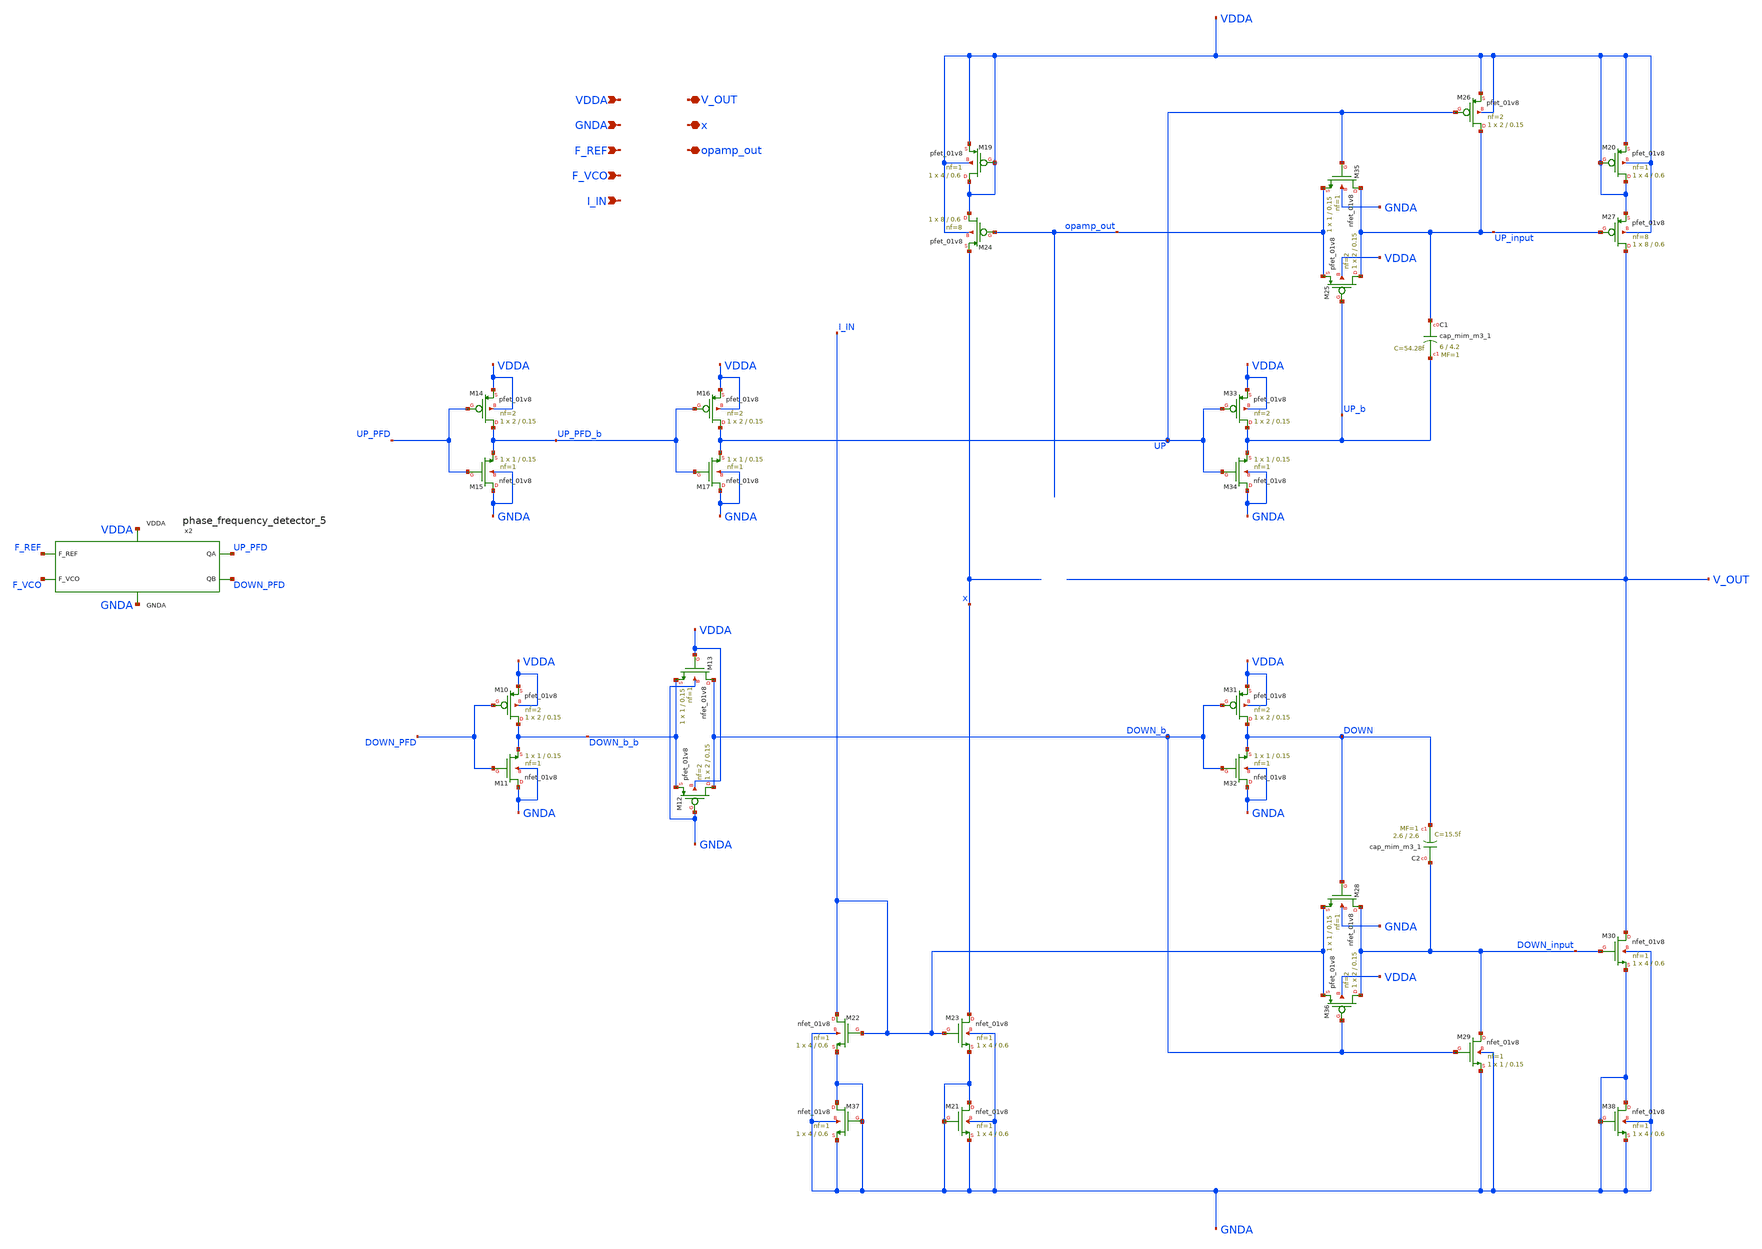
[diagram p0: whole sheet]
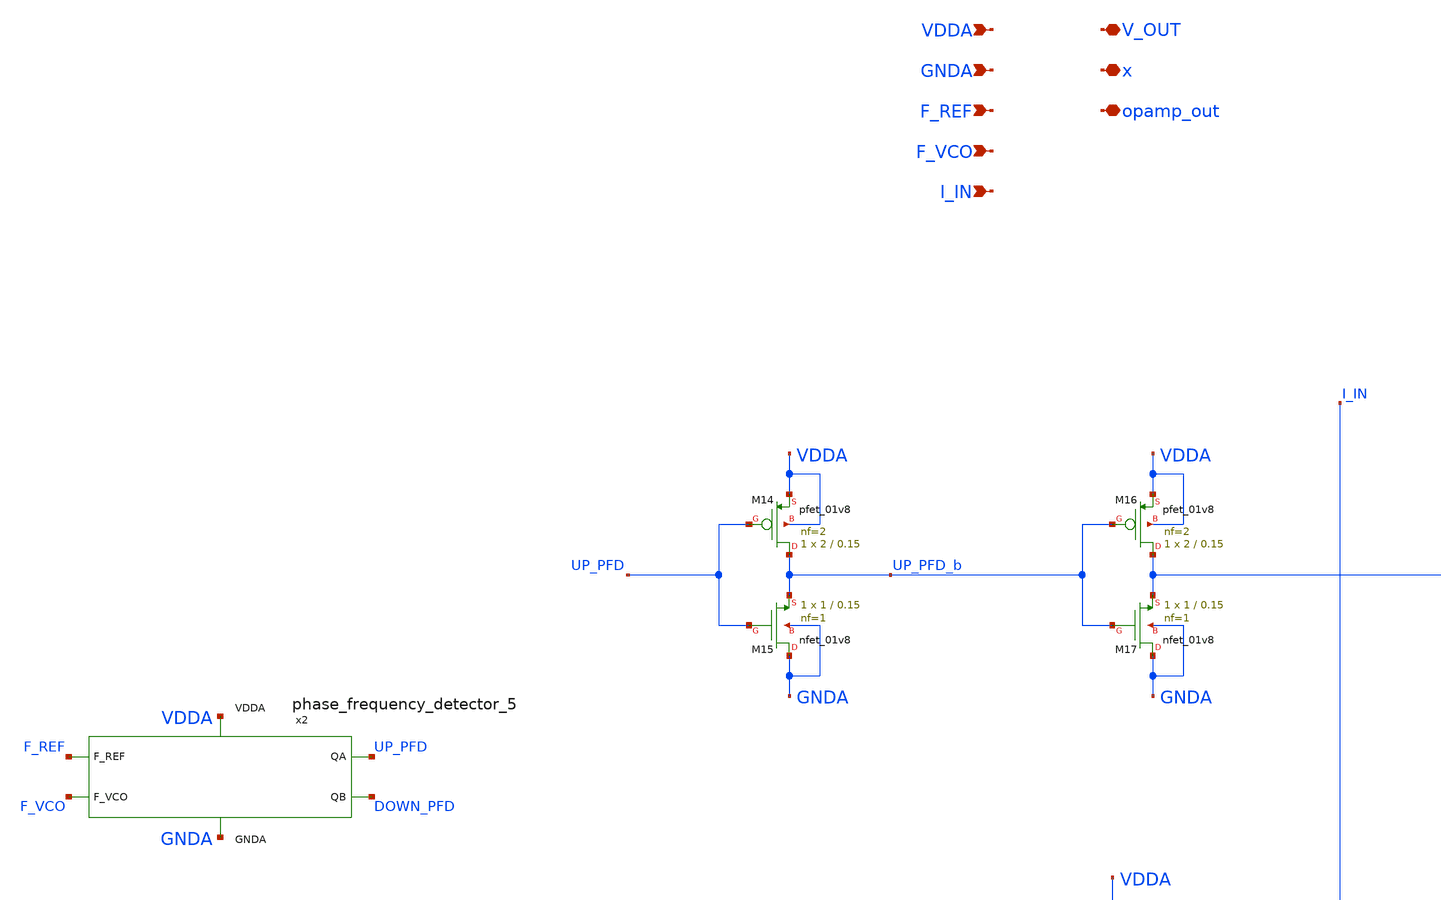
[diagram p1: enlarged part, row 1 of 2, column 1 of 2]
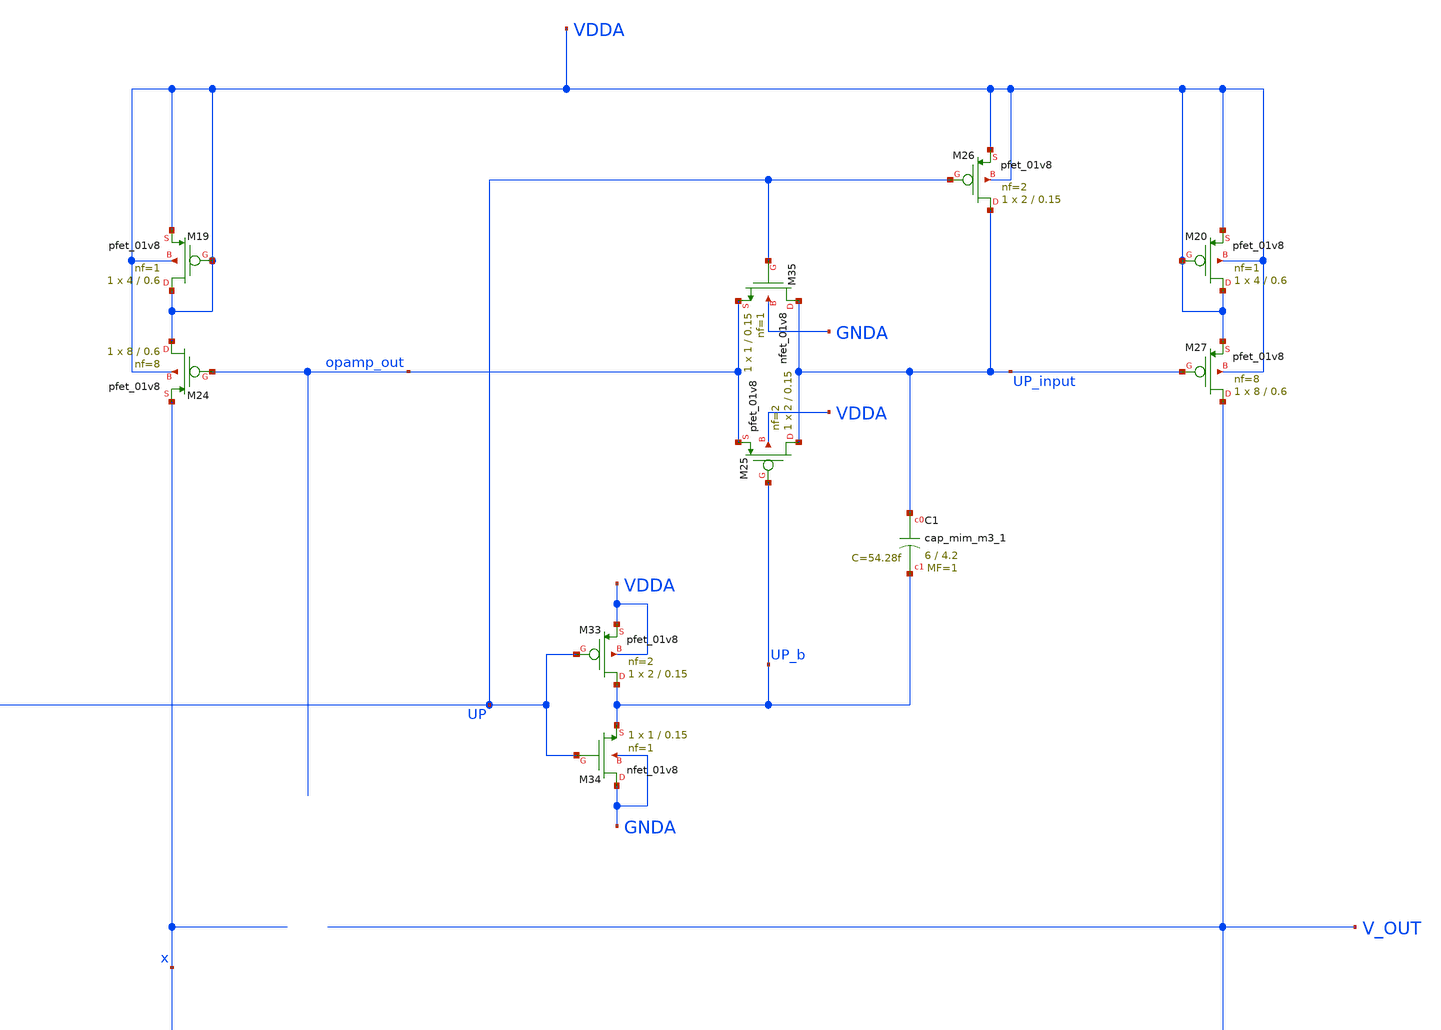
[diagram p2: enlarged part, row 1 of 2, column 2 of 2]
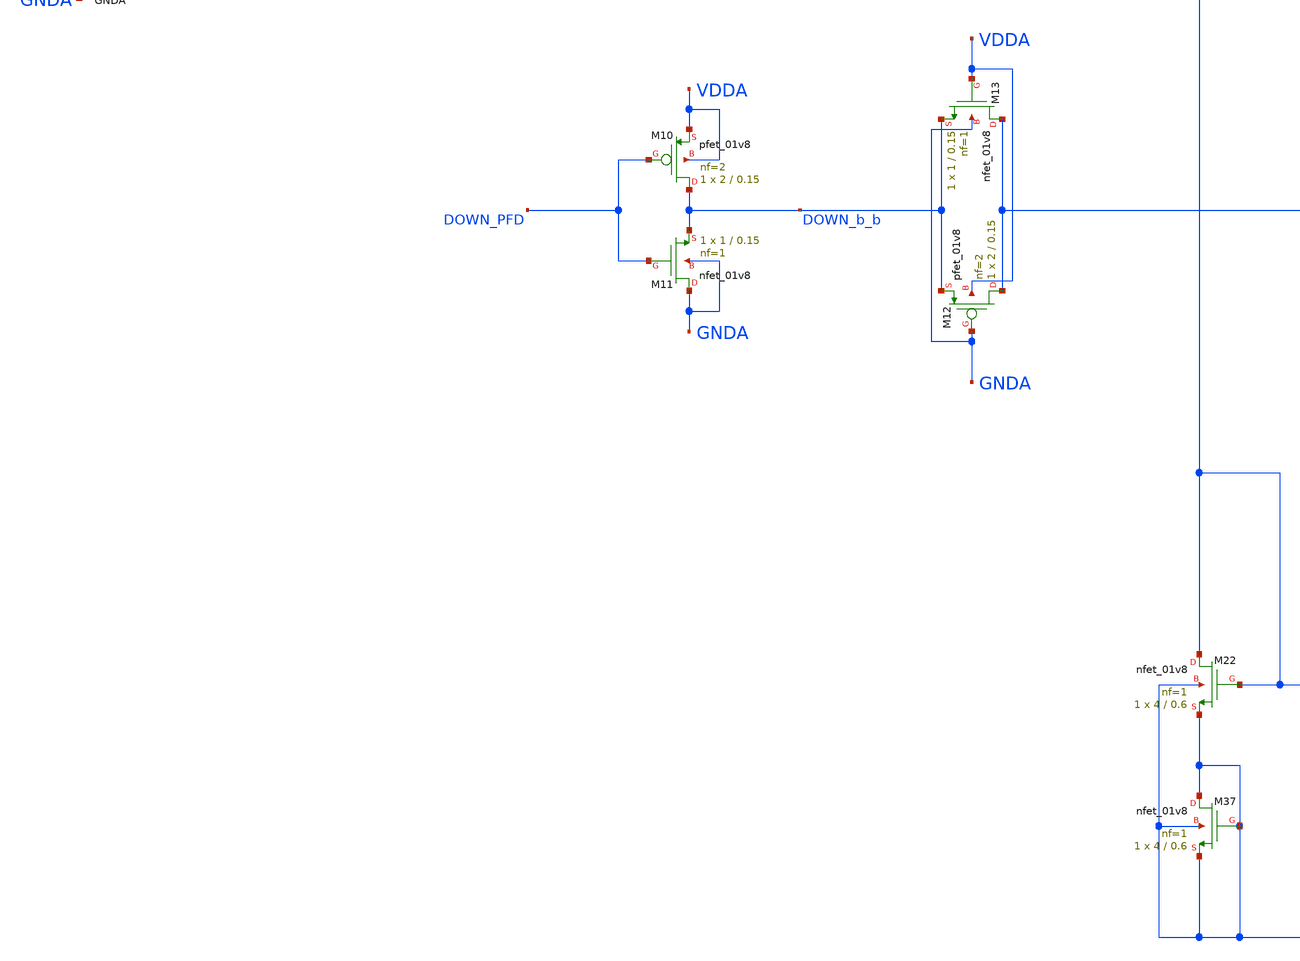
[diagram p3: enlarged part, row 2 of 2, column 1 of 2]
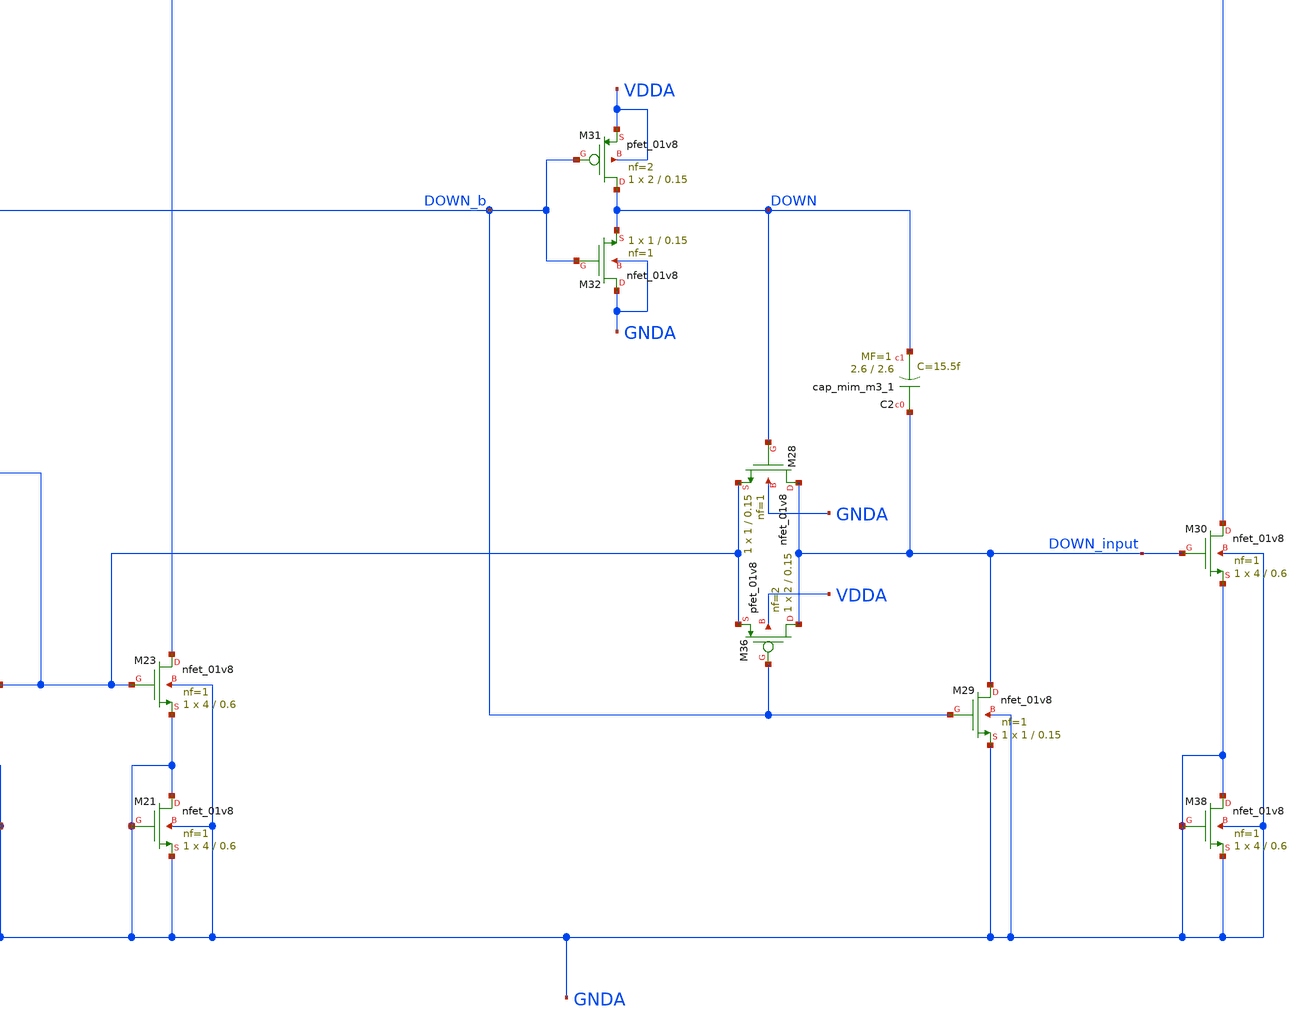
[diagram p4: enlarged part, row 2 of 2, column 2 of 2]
** sch_path: projects/pll/charge_pump/magic/pfd_cp_xschem_2.sch
**.subckt pfd_cp_xschem_2 VDDA GNDA F_REF F_VCO I_IN V_OUT x opamp_out
*.ipin VDDA
*.ipin GNDA
*.ipin F_REF
*.ipin F_VCO
*.ipin I_IN
*.iopin V_OUT
*.iopin x
*.iopin opamp_out
XM12 DOWN_b GNDA DOWN_b_b VDDA sky130_fd_pr__pfet_01v8 L=0.15 W=2 nf=2 ad='int((nf+1)/2) * W/nf * 0.29'
+ as='int((nf+2)/2) * W/nf * 0.29' pd='2*int((nf+1)/2) * (W/nf + 0.29)' ps='2*int((nf+2)/2) * (W/nf + 0.29)'
+ nrd='0.29 / W' nrs='0.29 / W' sa=0 sb=0 sd=0 mult=1 m=1
XM13 DOWN_b VDDA DOWN_b_b GNDA sky130_fd_pr__nfet_01v8 L=0.15 W=1 nf=1 ad='int((nf+1)/2) * W/nf * 0.29'
+ as='int((nf+2)/2) * W/nf * 0.29' pd='2*int((nf+1)/2) * (W/nf + 0.29)' ps='2*int((nf+2)/2) * (W/nf + 0.29)'
+ nrd='0.29 / W' nrs='0.29 / W' sa=0 sb=0 sd=0 mult=1 m=1
XM10 DOWN_b_b DOWN_PFD VDDA VDDA sky130_fd_pr__pfet_01v8 L=0.15 W=2 nf=2 ad='int((nf+1)/2) * W/nf * 0.29'
+ as='int((nf+2)/2) * W/nf * 0.29' pd='2*int((nf+1)/2) * (W/nf + 0.29)' ps='2*int((nf+2)/2) * (W/nf + 0.29)'
+ nrd='0.29 / W' nrs='0.29 / W' sa=0 sb=0 sd=0 mult=1 m=1
XM11 GNDA DOWN_PFD DOWN_b_b GNDA sky130_fd_pr__nfet_01v8 L=0.15 W=1 nf=1 ad='int((nf+1)/2) * W/nf * 0.29'
+ as='int((nf+2)/2) * W/nf * 0.29' pd='2*int((nf+1)/2) * (W/nf + 0.29)' ps='2*int((nf+2)/2) * (W/nf + 0.29)'
+ nrd='0.29 / W' nrs='0.29 / W' sa=0 sb=0 sd=0 mult=1 m=1
XM14 UP_PFD_b UP_PFD VDDA VDDA sky130_fd_pr__pfet_01v8 L=0.15 W=2 nf=2 ad='int((nf+1)/2) * W/nf * 0.29'
+ as='int((nf+2)/2) * W/nf * 0.29' pd='2*int((nf+1)/2) * (W/nf + 0.29)' ps='2*int((nf+2)/2) * (W/nf + 0.29)'
+ nrd='0.29 / W' nrs='0.29 / W' sa=0 sb=0 sd=0 mult=1 m=1
XM15 GNDA UP_PFD UP_PFD_b GNDA sky130_fd_pr__nfet_01v8 L=0.15 W=1 nf=1 ad='int((nf+1)/2) * W/nf * 0.29'
+ as='int((nf+2)/2) * W/nf * 0.29' pd='2*int((nf+1)/2) * (W/nf + 0.29)' ps='2*int((nf+2)/2) * (W/nf + 0.29)'
+ nrd='0.29 / W' nrs='0.29 / W' sa=0 sb=0 sd=0 mult=1 m=1
XM16 UP UP_PFD_b VDDA VDDA sky130_fd_pr__pfet_01v8 L=0.15 W=2 nf=2 ad='int((nf+1)/2) * W/nf * 0.29' as='int((nf+2)/2) * W/nf * 0.29'
+ pd='2*int((nf+1)/2) * (W/nf + 0.29)' ps='2*int((nf+2)/2) * (W/nf + 0.29)' nrd='0.29 / W' nrs='0.29 / W'
+ sa=0 sb=0 sd=0 mult=1 m=1
XM17 GNDA UP_PFD_b UP GNDA sky130_fd_pr__nfet_01v8 L=0.15 W=1 nf=1 ad='int((nf+1)/2) * W/nf * 0.29' as='int((nf+2)/2) * W/nf * 0.29'
+ pd='2*int((nf+1)/2) * (W/nf + 0.29)' ps='2*int((nf+2)/2) * (W/nf + 0.29)' nrd='0.29 / W' nrs='0.29 / W'
+ sa=0 sb=0 sd=0 mult=1 m=1
XM22 I_IN I_IN GNDA GNDA sky130_fd_pr__nfet_01v8 L=0.6 W=4 nf=1 ad='int((nf+1)/2) * W/nf * 0.29' as='int((nf+2)/2) * W/nf * 0.29'
+ pd='2*int((nf+1)/2) * (W/nf + 0.29)' ps='2*int((nf+2)/2) * (W/nf + 0.29)' nrd='0.29 / W' nrs='0.29 / W'
+ sa=0 sb=0 sd=0 mult=1 m=1
XM23 x I_IN GNDA GNDA sky130_fd_pr__nfet_01v8 L=0.6 W=4 nf=1 ad='int((nf+1)/2) * W/nf * 0.29' as='int((nf+2)/2) * W/nf * 0.29'
+ pd='2*int((nf+1)/2) * (W/nf + 0.29)' ps='2*int((nf+2)/2) * (W/nf + 0.29)' nrd='0.29 / W' nrs='0.29 / W'
+ sa=0 sb=0 sd=0 mult=1 m=1
XM24 VDDA opamp_out x VDDA sky130_fd_pr__pfet_01v8 L=0.6 W=8 nf=8 ad='int((nf+1)/2) * W/nf * 0.29' as='int((nf+2)/2) * W/nf * 0.29'
+ pd='2*int((nf+1)/2) * (W/nf + 0.29)' ps='2*int((nf+2)/2) * (W/nf + 0.29)' nrd='0.29 / W' nrs='0.29 / W'
+ sa=0 sb=0 sd=0 mult=1 m=1
XM25 UP_input UP_b opamp_out VDDA sky130_fd_pr__pfet_01v8 L=0.15 W=2 nf=2 ad='int((nf+1)/2) * W/nf * 0.29'
+ as='int((nf+2)/2) * W/nf * 0.29' pd='2*int((nf+1)/2) * (W/nf + 0.29)' ps='2*int((nf+2)/2) * (W/nf + 0.29)'
+ nrd='0.29 / W' nrs='0.29 / W' sa=0 sb=0 sd=0 mult=1 m=1
XM26 UP_input UP VDDA VDDA sky130_fd_pr__pfet_01v8 L=0.15 W=2 nf=2 ad='int((nf+1)/2) * W/nf * 0.29' as='int((nf+2)/2) * W/nf * 0.29'
+ pd='2*int((nf+1)/2) * (W/nf + 0.29)' ps='2*int((nf+2)/2) * (W/nf + 0.29)' nrd='0.29 / W' nrs='0.29 / W'
+ sa=0 sb=0 sd=0 mult=1 m=1
XM27 V_OUT UP_input VDDA VDDA sky130_fd_pr__pfet_01v8 L=0.6 W=8 nf=8 ad='int((nf+1)/2) * W/nf * 0.29'
+ as='int((nf+2)/2) * W/nf * 0.29' pd='2*int((nf+1)/2) * (W/nf + 0.29)' ps='2*int((nf+2)/2) * (W/nf + 0.29)'
+ nrd='0.29 / W' nrs='0.29 / W' sa=0 sb=0 sd=0 mult=1 m=1
XM28 DOWN_input DOWN I_IN GNDA sky130_fd_pr__nfet_01v8 L=0.15 W=1 nf=1 ad='int((nf+1)/2) * W/nf * 0.29'
+ as='int((nf+2)/2) * W/nf * 0.29' pd='2*int((nf+1)/2) * (W/nf + 0.29)' ps='2*int((nf+2)/2) * (W/nf + 0.29)'
+ nrd='0.29 / W' nrs='0.29 / W' sa=0 sb=0 sd=0 mult=1 m=1
XM29 DOWN_input DOWN_b GNDA GNDA sky130_fd_pr__nfet_01v8 L=0.15 W=1 nf=1 ad='int((nf+1)/2) * W/nf * 0.29'
+ as='int((nf+2)/2) * W/nf * 0.29' pd='2*int((nf+1)/2) * (W/nf + 0.29)' ps='2*int((nf+2)/2) * (W/nf + 0.29)'
+ nrd='0.29 / W' nrs='0.29 / W' sa=0 sb=0 sd=0 mult=1 m=1
XM30 V_OUT DOWN_input GNDA GNDA sky130_fd_pr__nfet_01v8 L=0.6 W=4 nf=1 ad='int((nf+1)/2) * W/nf * 0.29'
+ as='int((nf+2)/2) * W/nf * 0.29' pd='2*int((nf+1)/2) * (W/nf + 0.29)' ps='2*int((nf+2)/2) * (W/nf + 0.29)'
+ nrd='0.29 / W' nrs='0.29 / W' sa=0 sb=0 sd=0 mult=1 m=1
XM31 DOWN DOWN_b VDDA VDDA sky130_fd_pr__pfet_01v8 L=0.15 W=2 nf=2 ad='int((nf+1)/2) * W/nf * 0.29' as='int((nf+2)/2) * W/nf * 0.29'
+ pd='2*int((nf+1)/2) * (W/nf + 0.29)' ps='2*int((nf+2)/2) * (W/nf + 0.29)' nrd='0.29 / W' nrs='0.29 / W'
+ sa=0 sb=0 sd=0 mult=1 m=1
XM32 GNDA DOWN_b DOWN GNDA sky130_fd_pr__nfet_01v8 L=0.15 W=1 nf=1 ad='int((nf+1)/2) * W/nf * 0.29' as='int((nf+2)/2) * W/nf * 0.29'
+ pd='2*int((nf+1)/2) * (W/nf + 0.29)' ps='2*int((nf+2)/2) * (W/nf + 0.29)' nrd='0.29 / W' nrs='0.29 / W'
+ sa=0 sb=0 sd=0 mult=1 m=1
XM33 UP_b UP VDDA VDDA sky130_fd_pr__pfet_01v8 L=0.15 W=2 nf=2 ad='int((nf+1)/2) * W/nf * 0.29' as='int((nf+2)/2) * W/nf * 0.29'
+ pd='2*int((nf+1)/2) * (W/nf + 0.29)' ps='2*int((nf+2)/2) * (W/nf + 0.29)' nrd='0.29 / W' nrs='0.29 / W'
+ sa=0 sb=0 sd=0 mult=1 m=1
XM34 GNDA UP UP_b GNDA sky130_fd_pr__nfet_01v8 L=0.15 W=1 nf=1 ad='int((nf+1)/2) * W/nf * 0.29' as='int((nf+2)/2) * W/nf * 0.29'
+ pd='2*int((nf+1)/2) * (W/nf + 0.29)' ps='2*int((nf+2)/2) * (W/nf + 0.29)' nrd='0.29 / W' nrs='0.29 / W'
+ sa=0 sb=0 sd=0 mult=1 m=1
XM35 UP_input UP opamp_out GNDA sky130_fd_pr__nfet_01v8 L=0.15 W=1 nf=1 ad='int((nf+1)/2) * W/nf * 0.29'
+ as='int((nf+2)/2) * W/nf * 0.29' pd='2*int((nf+1)/2) * (W/nf + 0.29)' ps='2*int((nf+2)/2) * (W/nf + 0.29)'
+ nrd='0.29 / W' nrs='0.29 / W' sa=0 sb=0 sd=0 mult=1 m=1
XM36 DOWN_input DOWN_b I_IN VDDA sky130_fd_pr__pfet_01v8 L=0.15 W=2 nf=2 ad='int((nf+1)/2) * W/nf * 0.29'
+ as='int((nf+2)/2) * W/nf * 0.29' pd='2*int((nf+1)/2) * (W/nf + 0.29)' ps='2*int((nf+2)/2) * (W/nf + 0.29)'
+ nrd='0.29 / W' nrs='0.29 / W' sa=0 sb=0 sd=0 mult=1 m=1
XC1 UP_input UP_b sky130_fd_pr__cap_mim_m3_1 W=6 L=4.2 MF=1 m=1
XC2 DOWN_input DOWN sky130_fd_pr__cap_mim_m3_1 W=2.6 L=2.6 MF=1 m=1
x2 F_REF F_VCO VDDA UP_PFD DOWN_PFD GNDA phase_frequency_detector_5
XM19 VDDA VDDA VDDA VDDA sky130_fd_pr__pfet_01v8 L=0.6 W=4 nf=1 ad='int((nf+1)/2) * W/nf * 0.29' as='int((nf+2)/2) * W/nf * 0.29'
+ pd='2*int((nf+1)/2) * (W/nf + 0.29)' ps='2*int((nf+2)/2) * (W/nf + 0.29)' nrd='0.29 / W' nrs='0.29 / W'
+ sa=0 sb=0 sd=0 mult=1 m=1
XM20 VDDA VDDA VDDA VDDA sky130_fd_pr__pfet_01v8 L=0.6 W=4 nf=1 ad='int((nf+1)/2) * W/nf * 0.29' as='int((nf+2)/2) * W/nf * 0.29'
+ pd='2*int((nf+1)/2) * (W/nf + 0.29)' ps='2*int((nf+2)/2) * (W/nf + 0.29)' nrd='0.29 / W' nrs='0.29 / W'
+ sa=0 sb=0 sd=0 mult=1 m=1
XM21 GNDA GNDA GNDA GNDA sky130_fd_pr__nfet_01v8 L=0.6 W=4 nf=1 ad='int((nf+1)/2) * W/nf * 0.29' as='int((nf+2)/2) * W/nf * 0.29'
+ pd='2*int((nf+1)/2) * (W/nf + 0.29)' ps='2*int((nf+2)/2) * (W/nf + 0.29)' nrd='0.29 / W' nrs='0.29 / W'
+ sa=0 sb=0 sd=0 mult=1 m=1
XM37 GNDA GNDA GNDA GNDA sky130_fd_pr__nfet_01v8 L=0.6 W=4 nf=1 ad='int((nf+1)/2) * W/nf * 0.29' as='int((nf+2)/2) * W/nf * 0.29'
+ pd='2*int((nf+1)/2) * (W/nf + 0.29)' ps='2*int((nf+2)/2) * (W/nf + 0.29)' nrd='0.29 / W' nrs='0.29 / W'
+ sa=0 sb=0 sd=0 mult=1 m=1
XM38 GNDA GNDA GNDA GNDA sky130_fd_pr__nfet_01v8 L=0.6 W=4 nf=1 ad='int((nf+1)/2) * W/nf * 0.29' as='int((nf+2)/2) * W/nf * 0.29'
+ pd='2*int((nf+1)/2) * (W/nf + 0.29)' ps='2*int((nf+2)/2) * (W/nf + 0.29)' nrd='0.29 / W' nrs='0.29 / W'
+ sa=0 sb=0 sd=0 mult=1 m=1
**.ends

* expanding   symbol:  phase_frequency_detector_5.sym # of pins=6
** sym_path: projects/pll/pfd/xschem_ngspice/phase_frequency_detector_5.sym
** sch_path: projects/pll/pfd/xschem_ngspice/phase_frequency_detector_5.sch
.subckt phase_frequency_detector_5 F_REF F_VCO VDDA QA QB GNDA
*.ipin F_REF
*.opin QA
*.ipin F_VCO
*.opin QB
*.ipin VDDA
*.ipin GNDA
x1 VDDA GNDA QA F_REF QA_b nor_pfd
x2 VDDA GNDA QB F_VCO QB_b nor_pfd
x3 VDDA GNDA QA_b E QA nor_pfd
x4 VDDA GNDA QB_b F QB nor_pfd
x5 VDDA GNDA E_b QA_b E nor_pfd
x6 VDDA GNDA F_b QB_b F nor_pfd
x7 VDDA GNDA E Reset E_b nor_pfd
x12 VDDA GNDA F Reset F_b nor_pfd
x8 VDDA GNDA QB QA before_Reset nand_pfd
x9 VDDA GNDA before_Reset net1 inv_pfd
x10 VDDA GNDA net1 net2 inv_pfd
x11 VDDA GNDA net2 net3 inv_pfd
x13 VDDA GNDA net3 net4 inv_pfd
x14 VDDA GNDA net4 Reset inv_pfd
.ends


* expanding   symbol:  /foss/designs/my_design/projects/pll/pfd/xschem_ngspice/nor_pfd.sym # of
*+ pins=5
** sym_path: projects/pll/pfd/xschem_ngspice/nor_pfd.sym
** sch_path: projects/pll/pfd/xschem_ngspice/nor_pfd.sch
.subckt nor_pfd VDDA GNDA A B Y
*.ipin A
*.opin Y
*.ipin VDDA
*.ipin GNDA
*.ipin B
XM4 net1 B VDDA VDDA sky130_fd_pr__pfet_01v8 L=0.15 W=2 nf=1 ad='int((nf+1)/2) * W/nf * 0.29' as='int((nf+2)/2) * W/nf * 0.29'
+ pd='2*int((nf+1)/2) * (W/nf + 0.29)' ps='2*int((nf+2)/2) * (W/nf + 0.29)' nrd='0.29 / W' nrs='0.29 / W'
+ sa=0 sb=0 sd=0 mult=1 m=1
XM2 GNDA B Y GNDA sky130_fd_pr__nfet_01v8 L=0.15 W=1 nf=1 ad='int((nf+1)/2) * W/nf * 0.29' as='int((nf+2)/2) * W/nf * 0.29'
+ pd='2*int((nf+1)/2) * (W/nf + 0.29)' ps='2*int((nf+2)/2) * (W/nf + 0.29)' nrd='0.29 / W' nrs='0.29 / W'
+ sa=0 sb=0 sd=0 mult=1 m=1
XM1 GNDA A Y GNDA sky130_fd_pr__nfet_01v8 L=0.15 W=1 nf=1 ad='int((nf+1)/2) * W/nf * 0.29' as='int((nf+2)/2) * W/nf * 0.29'
+ pd='2*int((nf+1)/2) * (W/nf + 0.29)' ps='2*int((nf+2)/2) * (W/nf + 0.29)' nrd='0.29 / W' nrs='0.29 / W'
+ sa=0 sb=0 sd=0 mult=1 m=1
XM3 Y A net1 VDDA sky130_fd_pr__pfet_01v8 L=0.15 W=2 nf=1 ad='int((nf+1)/2) * W/nf * 0.29' as='int((nf+2)/2) * W/nf * 0.29'
+ pd='2*int((nf+1)/2) * (W/nf + 0.29)' ps='2*int((nf+2)/2) * (W/nf + 0.29)' nrd='0.29 / W' nrs='0.29 / W'
+ sa=0 sb=0 sd=0 mult=1 m=1
.ends


* expanding   symbol:  /foss/designs/my_design/projects/pll/pfd/xschem_ngspice/nand_pfd.sym # of
*+ pins=5
** sym_path: projects/pll/pfd/xschem_ngspice/nand_pfd.sym
** sch_path: projects/pll/pfd/xschem_ngspice/nand_pfd.sch
.subckt nand_pfd VDDA GNDA A B Y
*.ipin A
*.opin Y
*.ipin VDDA
*.ipin GNDA
*.ipin B
XM4 Y B VDDA VDDA sky130_fd_pr__pfet_01v8 L=0.15 W=1 nf=2 ad='int((nf+1)/2) * W/nf * 0.29' as='int((nf+2)/2) * W/nf * 0.29'
+ pd='2*int((nf+1)/2) * (W/nf + 0.29)' ps='2*int((nf+2)/2) * (W/nf + 0.29)' nrd='0.29 / W' nrs='0.29 / W'
+ sa=0 sb=0 sd=0 mult=1 m=1
XM2 net1 B Y GNDA sky130_fd_pr__nfet_01v8 L=0.15 W=0.5 nf=1 ad='int((nf+1)/2) * W/nf * 0.29' as='int((nf+2)/2) * W/nf * 0.29'
+ pd='2*int((nf+1)/2) * (W/nf + 0.29)' ps='2*int((nf+2)/2) * (W/nf + 0.29)' nrd='0.29 / W' nrs='0.29 / W'
+ sa=0 sb=0 sd=0 mult=1 m=1
XM1 GNDA A net1 GNDA sky130_fd_pr__nfet_01v8 L=0.15 W=0.5 nf=1 ad='int((nf+1)/2) * W/nf * 0.29' as='int((nf+2)/2) * W/nf * 0.29'
+ pd='2*int((nf+1)/2) * (W/nf + 0.29)' ps='2*int((nf+2)/2) * (W/nf + 0.29)' nrd='0.29 / W' nrs='0.29 / W'
+ sa=0 sb=0 sd=0 mult=1 m=1
XM3 Y A VDDA VDDA sky130_fd_pr__pfet_01v8 L=0.15 W=1 nf=2 ad='int((nf+1)/2) * W/nf * 0.29' as='int((nf+2)/2) * W/nf * 0.29'
+ pd='2*int((nf+1)/2) * (W/nf + 0.29)' ps='2*int((nf+2)/2) * (W/nf + 0.29)' nrd='0.29 / W' nrs='0.29 / W'
+ sa=0 sb=0 sd=0 mult=1 m=1
.ends


* expanding   symbol:  /foss/designs/my_design/projects/pll/pfd/xschem_ngspice/inv_pfd.sym # of
*+ pins=4
** sym_path: projects/ASU/EEE572/schematic/inv_pfd.sym
** sch_path: projects/ASU/EEE572/schematic/inv_pfd.sch
.subckt inv_pfd VDDA GNDA A Y
*.ipin A
*.opin Y
*.ipin VDDA
*.ipin GNDA
XM2 Y A VDDA VDDA sky130_fd_pr__pfet_01v8 L=0.15 W=2 nf=1 ad='int((nf+1)/2) * W/nf * 0.29' as='int((nf+2)/2) * W/nf * 0.29'
+ pd='2*int((nf+1)/2) * (W/nf + 0.29)' ps='2*int((nf+2)/2) * (W/nf + 0.29)' nrd='0.29 / W' nrs='0.29 / W'
+ sa=0 sb=0 sd=0 mult=1 m=1
XM1 GNDA A Y GNDA sky130_fd_pr__nfet_01v8 L=0.15 W=1 nf=1 ad='int((nf+1)/2) * W/nf * 0.29' as='int((nf+2)/2) * W/nf * 0.29'
+ pd='2*int((nf+1)/2) * (W/nf + 0.29)' ps='2*int((nf+2)/2) * (W/nf + 0.29)' nrd='0.29 / W' nrs='0.29 / W'
+ sa=0 sb=0 sd=0 mult=1 m=1
.ends

.end
